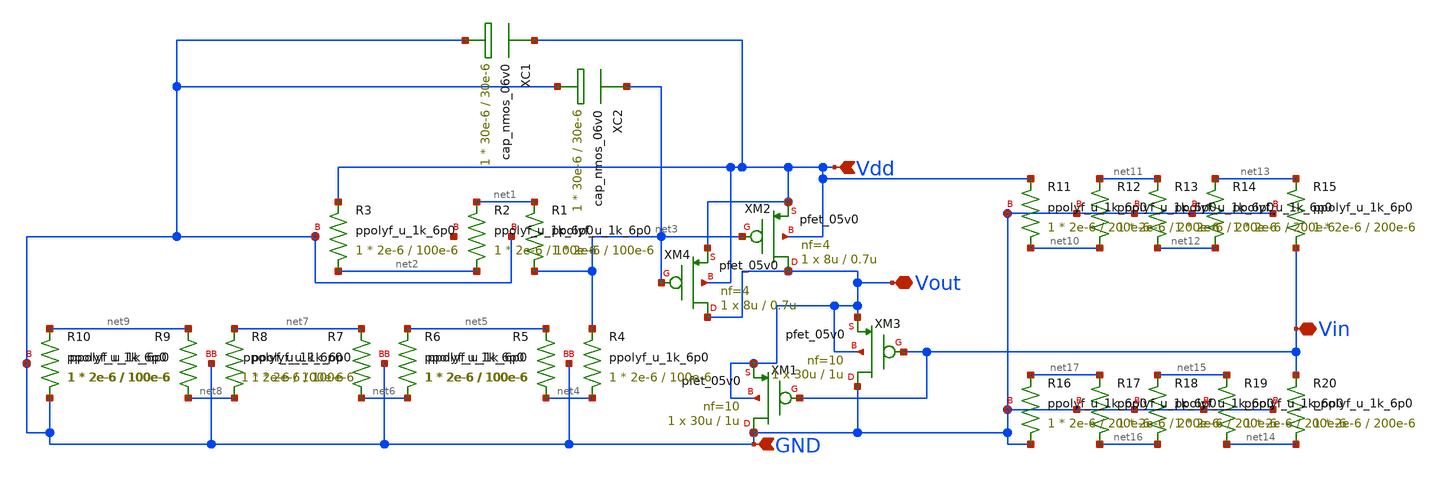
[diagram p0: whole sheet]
** sch_path: RN_buffer/RN_buffer.sch
**.subckt RN_buffer Vdd GND Vin Vout
*.ipin Vdd
*.ipin GND
*.iopin Vin
*.iopin Vout
XM1 GND Vin Vout Vout pfet_05v0 L=1u W=30u nf=10 ad='int((nf+1)/2) * W/nf * 0.18u' as='int((nf+2)/2) * W/nf * 0.18u'
+ pd='2*int((nf+1)/2) * (W/nf + 0.18u)' ps='2*int((nf+2)/2) * (W/nf + 0.18u)' nrd='0.18u / W' nrs='0.18u / W'
+ sa=0 sb=0 sd=0 m=1
XM2 Vout net3 Vdd Vdd pfet_05v0 L=0.7u W=8u nf=4 ad='int((nf+1)/2) * W/nf * 0.18u' as='int((nf+2)/2) * W/nf * 0.18u'
+ pd='2*int((nf+1)/2) * (W/nf + 0.18u)' ps='2*int((nf+2)/2) * (W/nf + 0.18u)' nrd='0.18u / W' nrs='0.18u / W'
+ sa=0 sb=0 sd=0 m=1
XM3 GND Vin Vout Vout pfet_05v0 L=1u W=30u nf=10 ad='int((nf+1)/2) * W/nf * 0.18u' as='int((nf+2)/2) * W/nf * 0.18u'
+ pd='2*int((nf+1)/2) * (W/nf + 0.18u)' ps='2*int((nf+2)/2) * (W/nf + 0.18u)' nrd='0.18u / W' nrs='0.18u / W'
+ sa=0 sb=0 sd=0 m=1
XM4 Vout net3 Vdd Vdd pfet_05v0 L=0.7u W=8u nf=4 ad='int((nf+1)/2) * W/nf * 0.18u' as='int((nf+2)/2) * W/nf * 0.18u'
+ pd='2*int((nf+1)/2) * (W/nf + 0.18u)' ps='2*int((nf+2)/2) * (W/nf + 0.18u)' nrd='0.18u / W' nrs='0.18u / W'
+ sa=0 sb=0 sd=0 m=1
XR11 net10 Vdd GND ppolyf_u_1k_6p0 r_width=2e-6 r_length=200e-6 m=1
XR12 net10 net11 GND ppolyf_u_1k_6p0 r_width=2e-6 r_length=200e-6 m=1
XR13 net12 net11 GND ppolyf_u_1k_6p0 r_width=2e-6 r_length=200e-6 m=1
XR14 net12 net13 GND ppolyf_u_1k_6p0 r_width=2e-6 r_length=200e-6 m=1
XR15 Vin net13 GND ppolyf_u_1k_6p0 r_width=2e-6 r_length=200e-6 m=1
XR16 GND net17 GND ppolyf_u_1k_6p0 r_width=2e-6 r_length=200e-6 m=1
XR17 net16 net17 GND ppolyf_u_1k_6p0 r_width=2e-6 r_length=200e-6 m=1
XR18 net16 net15 GND ppolyf_u_1k_6p0 r_width=2e-6 r_length=200e-6 m=1
XR19 net14 net15 GND ppolyf_u_1k_6p0 r_width=2e-6 r_length=200e-6 m=1
XR20 net14 Vin GND ppolyf_u_1k_6p0 r_width=2e-6 r_length=200e-6 m=1
XR1 net3 net1 GND ppolyf_u_1k_6p0 r_width=2e-6 r_length=100e-6 m=1
XR2 net2 net1 net18 ppolyf_u_1k_6p0 r_width=2e-6 r_length=100e-6 m=1
XR3 net2 Vdd GND ppolyf_u_1k_6p0 r_width=2e-6 r_length=100e-6 m=1
XR4 net4 net3 GND ppolyf_u_1k_6p0 r_width=2e-6 r_length=100e-6 m=1
XR5 net4 net5 GND ppolyf_u_1k_6p0 r_width=2e-6 r_length=100e-6 m=1
XR6 net6 net5 GND ppolyf_u_1k_6p0 r_width=2e-6 r_length=100e-6 m=1
XR7 net6 net7 GND ppolyf_u_1k_6p0 r_width=2e-6 r_length=100e-6 m=1
XR8 net8 net7 GND ppolyf_u_1k_6p0 r_width=2e-6 r_length=100e-6 m=1
XR9 net8 net9 GND ppolyf_u_1k_6p0 r_width=2e-6 r_length=100e-6 m=1
XR10 GND net9 GND ppolyf_u_1k_6p0 r_width=2e-6 r_length=100e-6 m=1
XC1 Vdd GND cap_nmos_06v0 c_width=30e-6 c_length=30e-6 m=1
XC2 net3 GND cap_nmos_06v0 c_width=30e-6 c_length=30e-6 m=1
**.ends
.end
